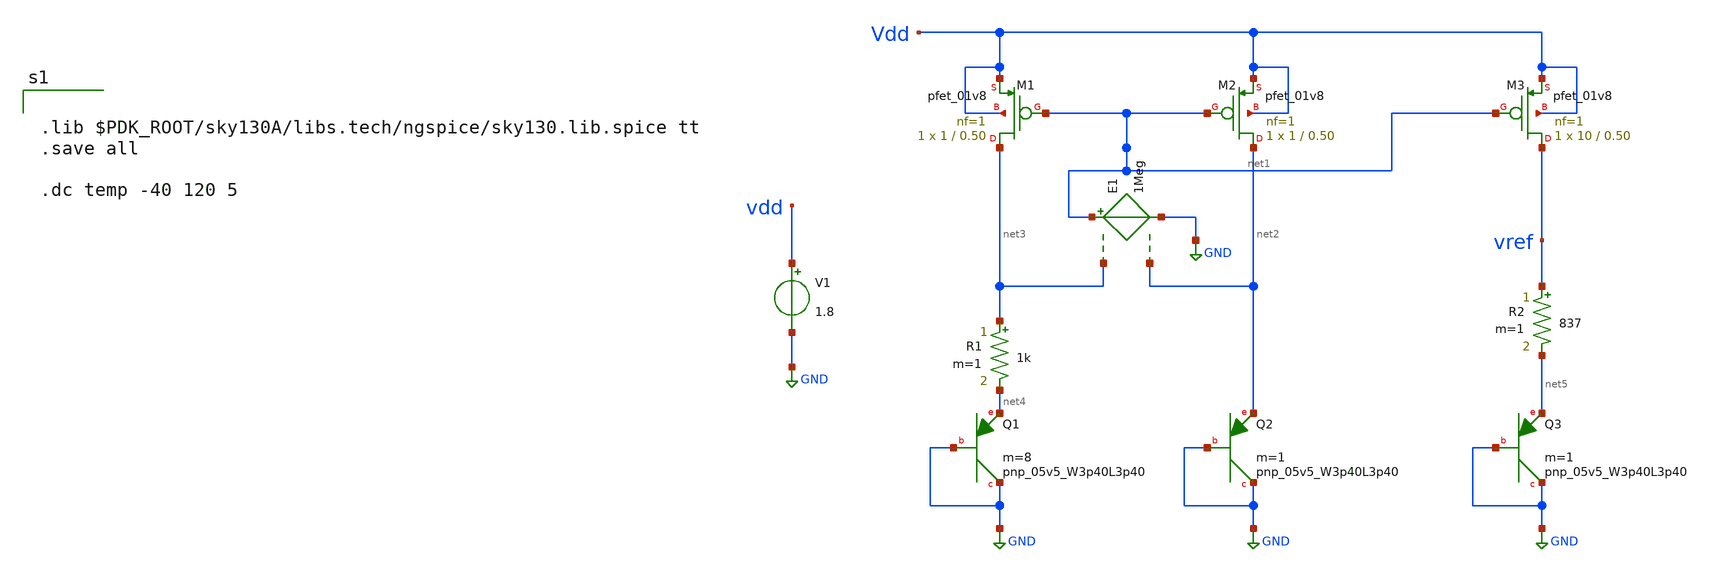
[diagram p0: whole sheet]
** sch_path: Bandgap/schem.sch
**.subckt schem
R1 net3 net4 1k m=1
XQ1 GND GND net4 sky130_fd_pr__pnp_05v5_W3p40L3p40 m=8
XQ2 GND GND net2 sky130_fd_pr__pnp_05v5_W3p40L3p40 m=1
E1 net1 GND net3 net2 1Meg
V1 vdd GND 1.8
R2 vref net5 837 m=1
XQ3 GND GND net5 sky130_fd_pr__pnp_05v5_W3p40L3p40 m=1
XM1 net3 net1 Vdd Vdd sky130_fd_pr__pfet_01v8 L=0.50 W=1 nf=1 ad='int((nf+1)/2) * W/nf * 0.29' as='int((nf+2)/2) * W/nf * 0.29'
+ pd='2*int((nf+1)/2) * (W/nf + 0.29)' ps='2*int((nf+2)/2) * (W/nf + 0.29)' nrd='0.29 / W' nrs='0.29 / W'
+ sa=0 sb=0 sd=0 mult=1 m=1
XM2 net2 net1 Vdd Vdd sky130_fd_pr__pfet_01v8 L=0.50 W=1 nf=1 ad='int((nf+1)/2) * W/nf * 0.29' as='int((nf+2)/2) * W/nf * 0.29'
+ pd='2*int((nf+1)/2) * (W/nf + 0.29)' ps='2*int((nf+2)/2) * (W/nf + 0.29)' nrd='0.29 / W' nrs='0.29 / W'
+ sa=0 sb=0 sd=0 mult=1 m=1
XM3 vref net1 Vdd Vdd sky130_fd_pr__pfet_01v8 L=0.50 W=10 nf=1 ad='int((nf+1)/2) * W/nf * 0.29' as='int((nf+2)/2) * W/nf * 0.29'
+ pd='2*int((nf+1)/2) * (W/nf + 0.29)' ps='2*int((nf+2)/2) * (W/nf + 0.29)' nrd='0.29 / W' nrs='0.29 / W'
+ sa=0 sb=0 sd=0 mult=1 m=1
**** begin user architecture code


.lib $PDK_ROOT/sky130A/libs.tech/ngspice/sky130.lib.spice tt
.save all

.dc temp -40 120 5


**** end user architecture code
**.ends
.GLOBAL GND
.end
